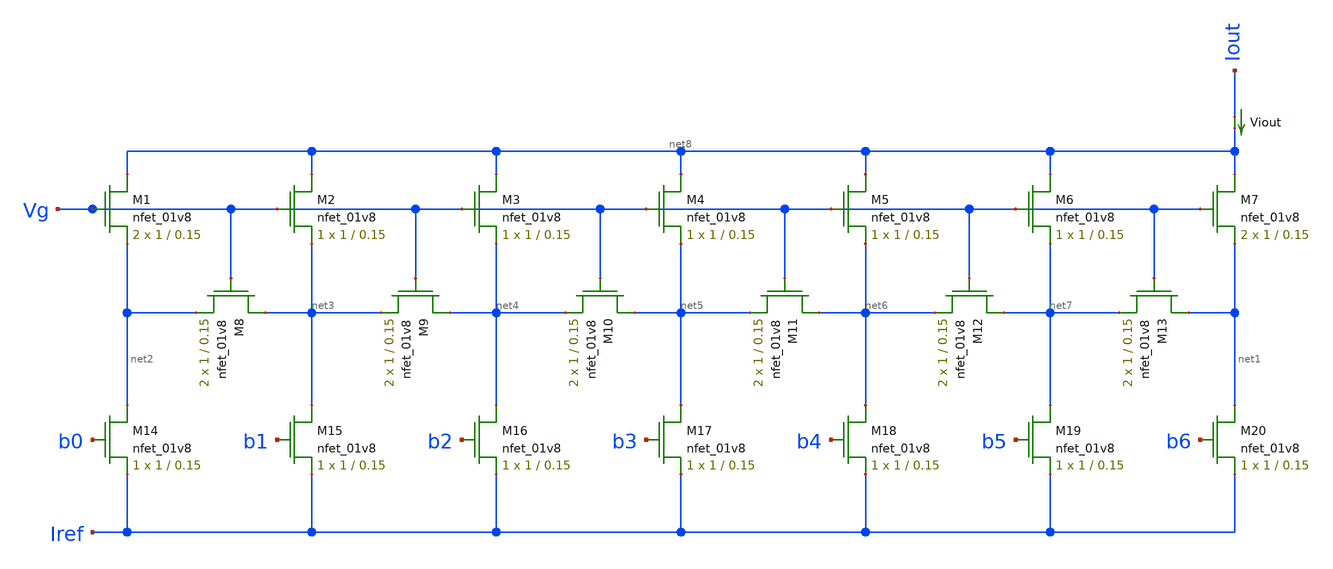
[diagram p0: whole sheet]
** sch_path: schematic/archive/dac_converter.sch
**.subckt dac_converter
XM1 net8 Vg net2 GND sky130_fd_pr__nfet_01v8 L=0.15 W=1 nf=1 ad='int((nf+1)/2) * W/nf * 0.29' as='int((nf+2)/2) * W/nf * 0.29'
+ pd='2*int((nf+1)/2) * (W/nf + 0.29)' ps='2*int((nf+2)/2) * (W/nf + 0.29)' nrd='0.29 / W' nrs='0.29 / W'
+ sa=0 sb=0 sd=0 mult=2 m=2
XM2 net8 Vg net3 GND sky130_fd_pr__nfet_01v8 L=0.15 W=1 nf=1 ad='int((nf+1)/2) * W/nf * 0.29' as='int((nf+2)/2) * W/nf * 0.29'
+ pd='2*int((nf+1)/2) * (W/nf + 0.29)' ps='2*int((nf+2)/2) * (W/nf + 0.29)' nrd='0.29 / W' nrs='0.29 / W'
+ sa=0 sb=0 sd=0 mult=1 m=1
XM3 net8 Vg net4 GND sky130_fd_pr__nfet_01v8 L=0.15 W=1 nf=1 ad='int((nf+1)/2) * W/nf * 0.29' as='int((nf+2)/2) * W/nf * 0.29'
+ pd='2*int((nf+1)/2) * (W/nf + 0.29)' ps='2*int((nf+2)/2) * (W/nf + 0.29)' nrd='0.29 / W' nrs='0.29 / W'
+ sa=0 sb=0 sd=0 mult=1 m=1
XM4 net8 Vg net5 GND sky130_fd_pr__nfet_01v8 L=0.15 W=1 nf=1 ad='int((nf+1)/2) * W/nf * 0.29' as='int((nf+2)/2) * W/nf * 0.29'
+ pd='2*int((nf+1)/2) * (W/nf + 0.29)' ps='2*int((nf+2)/2) * (W/nf + 0.29)' nrd='0.29 / W' nrs='0.29 / W'
+ sa=0 sb=0 sd=0 mult=1 m=1
XM5 net8 Vg net6 GND sky130_fd_pr__nfet_01v8 L=0.15 W=1 nf=1 ad='int((nf+1)/2) * W/nf * 0.29' as='int((nf+2)/2) * W/nf * 0.29'
+ pd='2*int((nf+1)/2) * (W/nf + 0.29)' ps='2*int((nf+2)/2) * (W/nf + 0.29)' nrd='0.29 / W' nrs='0.29 / W'
+ sa=0 sb=0 sd=0 mult=1 m=1
XM6 net8 Vg net7 GND sky130_fd_pr__nfet_01v8 L=0.15 W=1 nf=1 ad='int((nf+1)/2) * W/nf * 0.29' as='int((nf+2)/2) * W/nf * 0.29'
+ pd='2*int((nf+1)/2) * (W/nf + 0.29)' ps='2*int((nf+2)/2) * (W/nf + 0.29)' nrd='0.29 / W' nrs='0.29 / W'
+ sa=0 sb=0 sd=0 mult=1 m=1
XM7 net8 Vg net1 GND sky130_fd_pr__nfet_01v8 L=0.15 W=1 nf=1 ad='int((nf+1)/2) * W/nf * 0.29' as='int((nf+2)/2) * W/nf * 0.29'
+ pd='2*int((nf+1)/2) * (W/nf + 0.29)' ps='2*int((nf+2)/2) * (W/nf + 0.29)' nrd='0.29 / W' nrs='0.29 / W'
+ sa=0 sb=0 sd=0 mult=2 m=2
XM8 net3 Vg net2 GND sky130_fd_pr__nfet_01v8 L=0.15 W=1 nf=1 ad='int((nf+1)/2) * W/nf * 0.29' as='int((nf+2)/2) * W/nf * 0.29'
+ pd='2*int((nf+1)/2) * (W/nf + 0.29)' ps='2*int((nf+2)/2) * (W/nf + 0.29)' nrd='0.29 / W' nrs='0.29 / W'
+ sa=0 sb=0 sd=0 mult=2 m=2
XM14 net2 b0 Iref GND sky130_fd_pr__nfet_01v8 L=0.15 W=1 nf=1 ad='int((nf+1)/2) * W/nf * 0.29' as='int((nf+2)/2) * W/nf * 0.29'
+ pd='2*int((nf+1)/2) * (W/nf + 0.29)' ps='2*int((nf+2)/2) * (W/nf + 0.29)' nrd='0.29 / W' nrs='0.29 / W'
+ sa=0 sb=0 sd=0 mult=1 m=1
XM15 net3 b1 Iref GND sky130_fd_pr__nfet_01v8 L=0.15 W=1 nf=1 ad='int((nf+1)/2) * W/nf * 0.29' as='int((nf+2)/2) * W/nf * 0.29'
+ pd='2*int((nf+1)/2) * (W/nf + 0.29)' ps='2*int((nf+2)/2) * (W/nf + 0.29)' nrd='0.29 / W' nrs='0.29 / W'
+ sa=0 sb=0 sd=0 mult=1 m=1
XM16 net4 b2 Iref GND sky130_fd_pr__nfet_01v8 L=0.15 W=1 nf=1 ad='int((nf+1)/2) * W/nf * 0.29' as='int((nf+2)/2) * W/nf * 0.29'
+ pd='2*int((nf+1)/2) * (W/nf + 0.29)' ps='2*int((nf+2)/2) * (W/nf + 0.29)' nrd='0.29 / W' nrs='0.29 / W'
+ sa=0 sb=0 sd=0 mult=1 m=1
XM17 net5 b3 Iref GND sky130_fd_pr__nfet_01v8 L=0.15 W=1 nf=1 ad='int((nf+1)/2) * W/nf * 0.29' as='int((nf+2)/2) * W/nf * 0.29'
+ pd='2*int((nf+1)/2) * (W/nf + 0.29)' ps='2*int((nf+2)/2) * (W/nf + 0.29)' nrd='0.29 / W' nrs='0.29 / W'
+ sa=0 sb=0 sd=0 mult=1 m=1
XM18 net6 b4 Iref GND sky130_fd_pr__nfet_01v8 L=0.15 W=1 nf=1 ad='int((nf+1)/2) * W/nf * 0.29' as='int((nf+2)/2) * W/nf * 0.29'
+ pd='2*int((nf+1)/2) * (W/nf + 0.29)' ps='2*int((nf+2)/2) * (W/nf + 0.29)' nrd='0.29 / W' nrs='0.29 / W'
+ sa=0 sb=0 sd=0 mult=1 m=1
XM19 net7 b5 Iref GND sky130_fd_pr__nfet_01v8 L=0.15 W=1 nf=1 ad='int((nf+1)/2) * W/nf * 0.29' as='int((nf+2)/2) * W/nf * 0.29'
+ pd='2*int((nf+1)/2) * (W/nf + 0.29)' ps='2*int((nf+2)/2) * (W/nf + 0.29)' nrd='0.29 / W' nrs='0.29 / W'
+ sa=0 sb=0 sd=0 mult=1 m=1
XM20 net1 b6 Iref GND sky130_fd_pr__nfet_01v8 L=0.15 W=1 nf=1 ad='int((nf+1)/2) * W/nf * 0.29' as='int((nf+2)/2) * W/nf * 0.29'
+ pd='2*int((nf+1)/2) * (W/nf + 0.29)' ps='2*int((nf+2)/2) * (W/nf + 0.29)' nrd='0.29 / W' nrs='0.29 / W'
+ sa=0 sb=0 sd=0 mult=1 m=1
XM9 net4 Vg net3 GND sky130_fd_pr__nfet_01v8 L=0.15 W=1 nf=1 ad='int((nf+1)/2) * W/nf * 0.29' as='int((nf+2)/2) * W/nf * 0.29'
+ pd='2*int((nf+1)/2) * (W/nf + 0.29)' ps='2*int((nf+2)/2) * (W/nf + 0.29)' nrd='0.29 / W' nrs='0.29 / W'
+ sa=0 sb=0 sd=0 mult=2 m=2
XM10 net5 Vg net4 GND sky130_fd_pr__nfet_01v8 L=0.15 W=1 nf=1 ad='int((nf+1)/2) * W/nf * 0.29' as='int((nf+2)/2) * W/nf * 0.29'
+ pd='2*int((nf+1)/2) * (W/nf + 0.29)' ps='2*int((nf+2)/2) * (W/nf + 0.29)' nrd='0.29 / W' nrs='0.29 / W'
+ sa=0 sb=0 sd=0 mult=2 m=2
XM11 net6 Vg net5 GND sky130_fd_pr__nfet_01v8 L=0.15 W=1 nf=1 ad='int((nf+1)/2) * W/nf * 0.29' as='int((nf+2)/2) * W/nf * 0.29'
+ pd='2*int((nf+1)/2) * (W/nf + 0.29)' ps='2*int((nf+2)/2) * (W/nf + 0.29)' nrd='0.29 / W' nrs='0.29 / W'
+ sa=0 sb=0 sd=0 mult=2 m=2
XM12 net7 Vg net6 GND sky130_fd_pr__nfet_01v8 L=0.15 W=1 nf=1 ad='int((nf+1)/2) * W/nf * 0.29' as='int((nf+2)/2) * W/nf * 0.29'
+ pd='2*int((nf+1)/2) * (W/nf + 0.29)' ps='2*int((nf+2)/2) * (W/nf + 0.29)' nrd='0.29 / W' nrs='0.29 / W'
+ sa=0 sb=0 sd=0 mult=2 m=2
XM13 net1 Vg net7 GND sky130_fd_pr__nfet_01v8 L=0.15 W=1 nf=1 ad='int((nf+1)/2) * W/nf * 0.29' as='int((nf+2)/2) * W/nf * 0.29'
+ pd='2*int((nf+1)/2) * (W/nf + 0.29)' ps='2*int((nf+2)/2) * (W/nf + 0.29)' nrd='0.29 / W' nrs='0.29 / W'
+ sa=0 sb=0 sd=0 mult=2 m=2
Viout Iout net8 0
.save i(viout)
**.ends
.end
